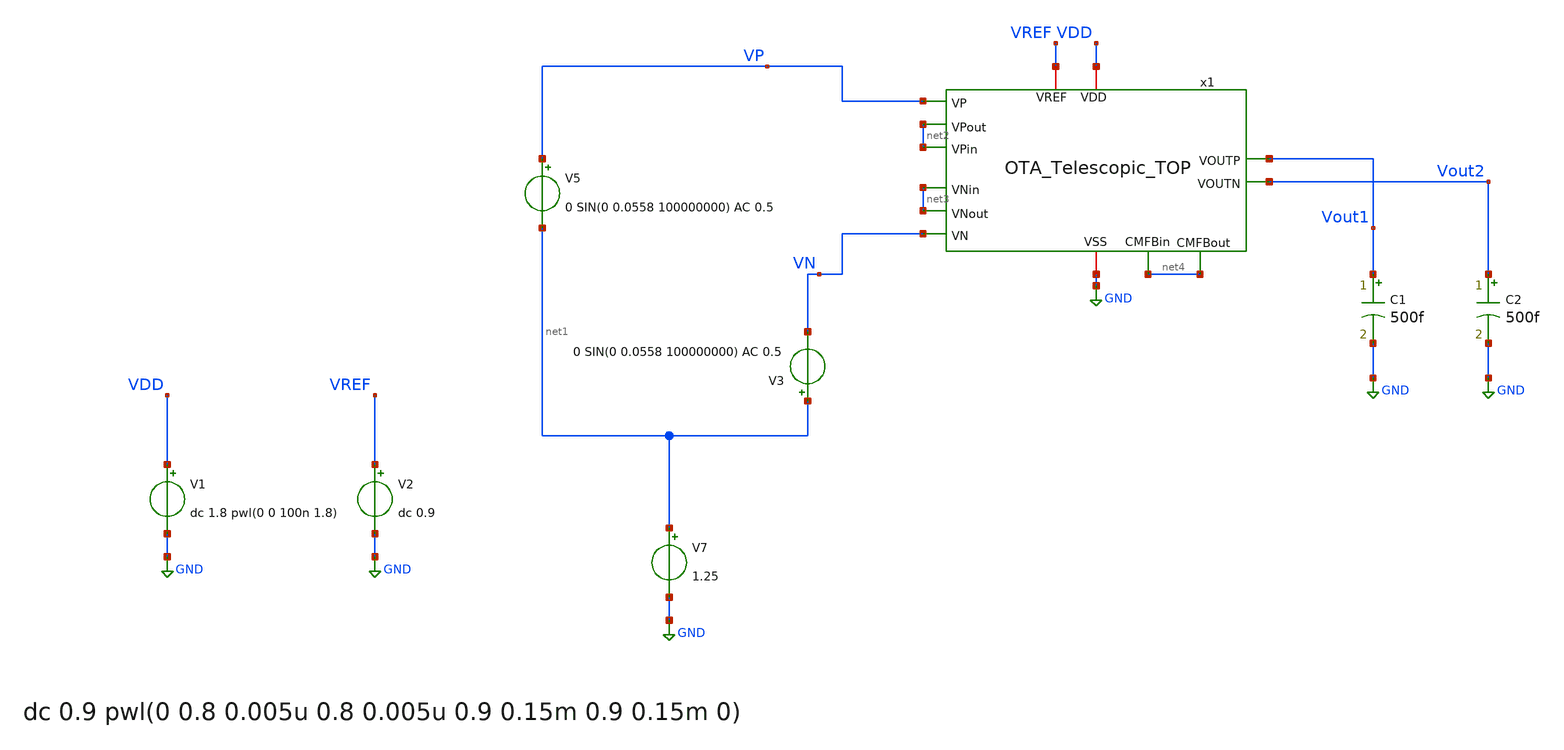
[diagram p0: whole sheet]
** sch_path: OTA_Telescopic/OTA_Telescopic_TOP_TB_StartUp.sch
**.subckt OTA_Telescopic_TOP_TB_StartUp
V7 net1 GND 1.25
V5 VP net1 0 SIN(0 0.0558 100000000) AC 0.5
V1 VDD GND dc 1.8 pwl(0 0 100n 1.8)
V2 VREF GND dc 0.9
C1 Vout1 GND 500f m=1
C2 Vout2 GND 500f m=1
V3 net1 VN 0 SIN(0 0.0558 100000000) AC 0.5
x1 VDD GND net2 VP net2 Vout2 Vout1 net3 net3 VN VREF net4 net4 OTA_Telescopic_TOP
**** begin user architecture code

** opencircuitdesign pdks install
.lib cornerMOSlv.lib mos_tt
.lib cornerRES.lib res_typ
.lib cornerCAP.lib cap_typ
.temp 65




.control

set wr_singlescale
set wr_vecnames

save all
tran 2.44140625p 1000n
*write NMOS_diode_large_signal.raw

let Vout1 = v(Vout1)
let Vout2 = v(Vout2)
let Vin = v(VP)-v(VN)
let VDD = v(VDD)

let Vout = v(Vout1)-v(Vout2)
wrdata Vout_tt_100_sym_DC.txt Vout
wrdata Vin_tt_100_sym_DC.txt Vin

plot Vin Vout
plot Vout1 Vout2
plot v(VP)-v(VN)
*plot v(VP) v(VN)
plot VDD

let Vo1 = v(x1.Vo1)
let Vo2 = v(x1.Vo2)

let Vo = Vo1-Vo2

wrdata Vo Vo

reset
noise v(Vout1) V5 dec 100 1 0.5e9 1
setplot noise1
*plot onoise_spectrum
setplot noise2
print onoise_total

.endc


**** end user architecture code
**.ends
.GLOBAL GND
.end
